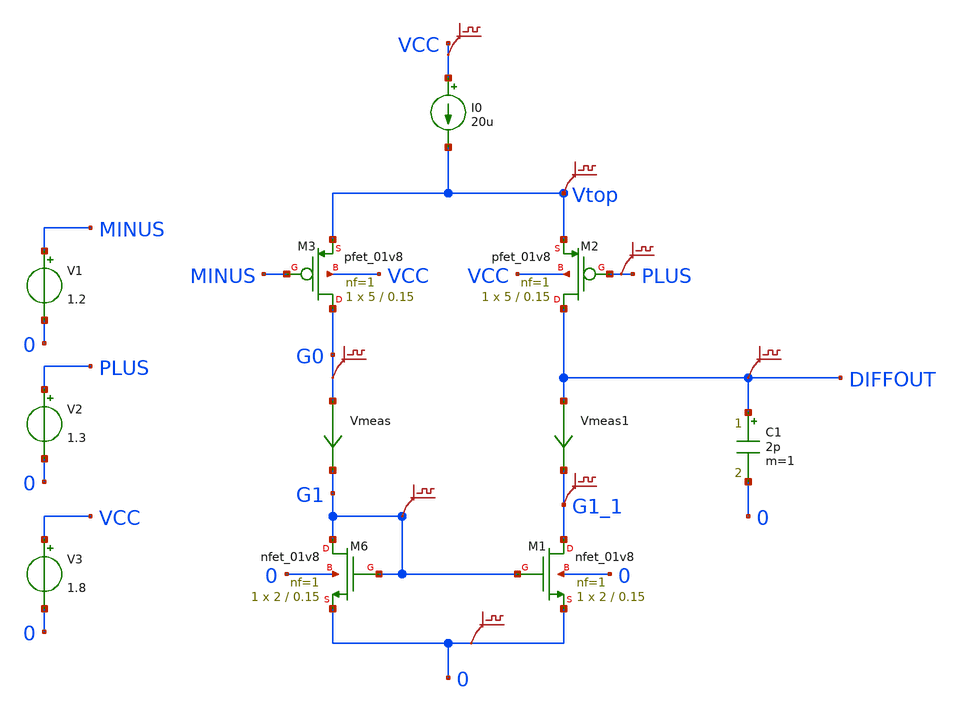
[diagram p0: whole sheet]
** sch_path: lib/xschem/LDO/Differential_Amp.sch
**.subckt Differential_Amp
V1 MINUS 0 1.2
V2 PLUS 0 1.3
V3 VCC 0 1.8
C1 DIFFOUT 0 2p m=1
XM6 G1 G1 0 0 sky130_fd_pr__nfet_01v8 L=0.15 W=2 nf=1 ad='int((nf+1)/2) * W/nf * 0.29' as='int((nf+2)/2) * W/nf * 0.29'
+ pd='2*int((nf+1)/2) * (W/nf + 0.29)' ps='2*int((nf+2)/2) * (W/nf + 0.29)' nrd='0.29 / W' nrs='0.29 / W'
+ sa=0 sb=0 sd=0 mult=1 m=1
XM1 G1_1 G1 0 0 sky130_fd_pr__nfet_01v8 L=0.15 W=2 nf=1 ad='int((nf+1)/2) * W/nf * 0.29' as='int((nf+2)/2) * W/nf * 0.29'
+ pd='2*int((nf+1)/2) * (W/nf + 0.29)' ps='2*int((nf+2)/2) * (W/nf + 0.29)' nrd='0.29 / W' nrs='0.29 / W'
+ sa=0 sb=0 sd=0 mult=1 m=1
XM2 DIFFOUT PLUS Vtop VCC sky130_fd_pr__pfet_01v8 L=0.15 W=5 nf=1 ad='int((nf+1)/2) * W/nf * 0.29' as='int((nf+2)/2) * W/nf * 0.29'
+ pd='2*int((nf+1)/2) * (W/nf + 0.29)' ps='2*int((nf+2)/2) * (W/nf + 0.29)' nrd='0.29 / W' nrs='0.29 / W'
+ sa=0 sb=0 sd=0 mult=1 m=1
XM3 G0 MINUS Vtop VCC sky130_fd_pr__pfet_01v8 L=0.15 W=5 nf=1 ad='int((nf+1)/2) * W/nf * 0.29' as='int((nf+2)/2) * W/nf * 0.29'
+ pd='2*int((nf+1)/2) * (W/nf + 0.29)' ps='2*int((nf+2)/2) * (W/nf + 0.29)' nrd='0.29 / W' nrs='0.29 / W'
+ sa=0 sb=0 sd=0 mult=1 m=1
I0 VCC Vtop 20u
Vmeas G0 G1 0
.save i(vmeas)
Vmeas1 DIFFOUT G1_1 0
.save i(vmeas1)
.save v(diffout)
.save v(vtop)
.save v(g1)
.save v(plus)
.save v(g0)
.save v(vcc)
.save v(g1_1)
.save v(0)
**** begin user architecture code

.lib $::SKYWATER_MODELS/sky130.lib.spice tt

.control
*op
*save all
*write Differential_Amp.raw
dc V2 1 1.8 0.01
plot v(PLUS) vs v(PLUS)
.endc

**** end user architecture code
**.ends
.end
